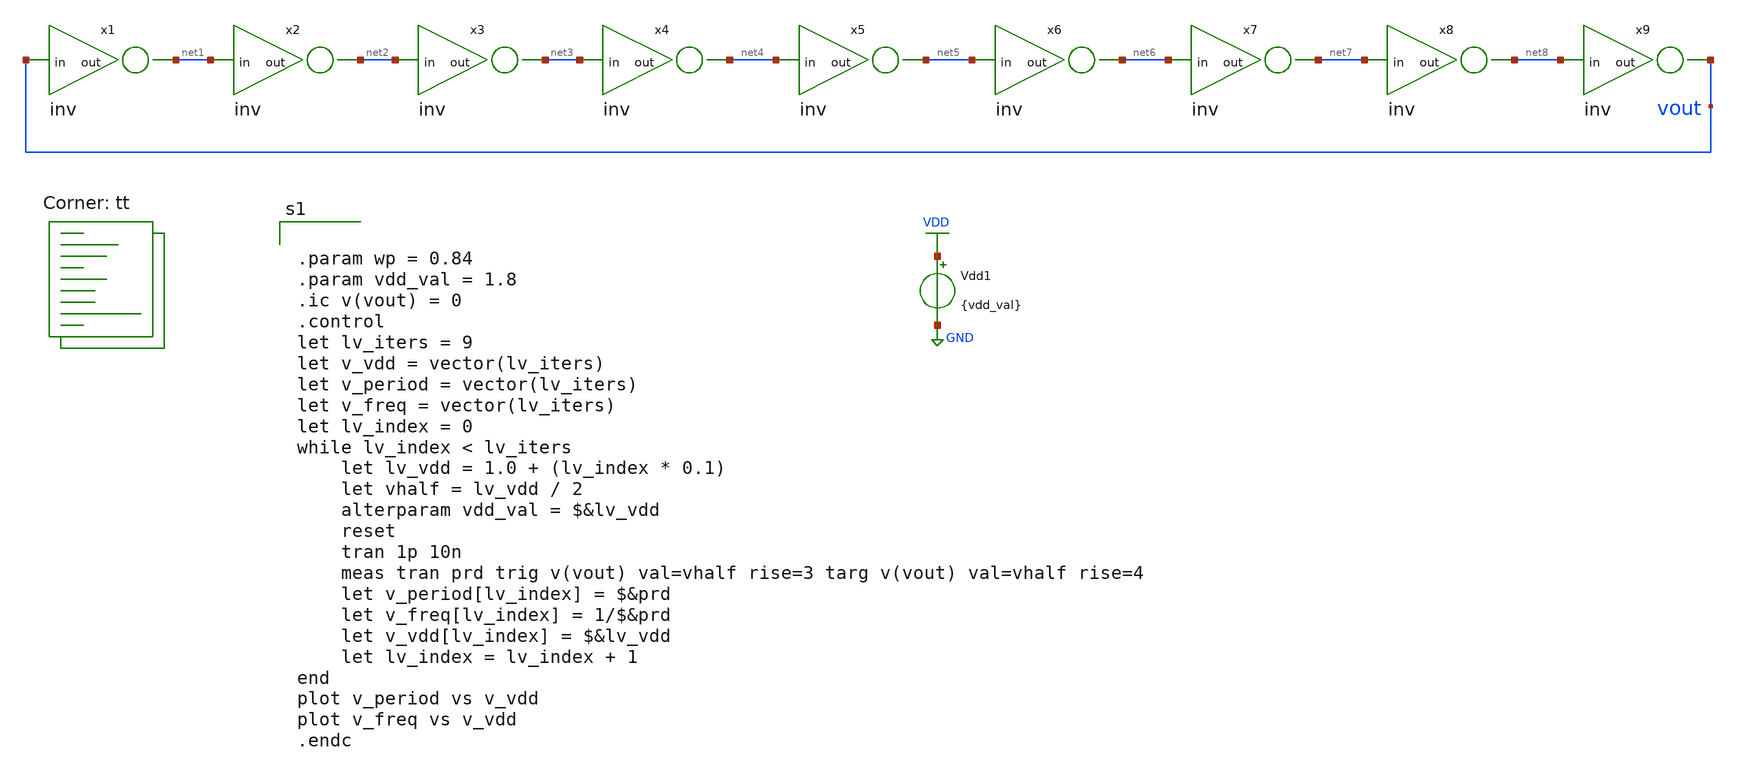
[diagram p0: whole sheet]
** sch_path: tut4/expt2/ro9.sch
**.subckt ro9
x1 net1 vout inv
x2 net2 net1 inv
x3 net3 net2 inv
x4 net4 net3 inv
x5 net5 net4 inv
x6 net6 net5 inv
x7 net7 net6 inv
Vdd1 VDD GND {vdd_val}
x8 net8 net7 inv
x9 vout net8 inv
**** begin user architecture code
.lib $::SKYWATER_MODELS/sky130.lib.spice tt


.param wp = 0.84
.param vdd_val = 1.8
.ic v(vout) = 0
.control
let lv_iters = 9
let v_vdd = vector(lv_iters)
let v_period = vector(lv_iters)
let v_freq = vector(lv_iters)
let lv_index = 0
while lv_index < lv_iters
	let lv_vdd = 1.0 + (lv_index * 0.1)
	let vhalf = lv_vdd / 2
	alterparam vdd_val = $&lv_vdd
	reset
	tran 1p 10n
	meas tran prd trig v(vout) val=vhalf rise=3 targ v(vout) val=vhalf rise=4
	let v_period[lv_index] = $&prd
	let v_freq[lv_index] = 1/$&prd
	let v_vdd[lv_index] = $&lv_vdd
	let lv_index = lv_index + 1
end
plot v_period vs v_vdd
plot v_freq vs v_vdd
.endc


**** end user architecture code
**.ends

* expanding   symbol:  /home/ee24s053/ee5311-2025/tut3/syms/inv.sym # of pins=2
** sym_path: tut3/syms/inv.sym
** sch_path: tut3/syms/inv.sch
.subckt inv out in
*.ipin in
*.opin out
XM1 out in VDD VDD sky130_fd_pr__pfet_01v8 L=0.15 W={wp} nf=1 ad='int((nf+1)/2) * W/nf * 0.29' as='int((nf+2)/2) * W/nf * 0.29'
+ pd='2*int((nf+1)/2) * (W/nf + 0.29)' ps='2*int((nf+2)/2) * (W/nf + 0.29)' nrd='0.29 / W' nrs='0.29 / W'
+ sa=0 sb=0 sd=0 mult=1 m=1
XM2 out in GND GND sky130_fd_pr__nfet_01v8 L=0.15 W=1 nf=1 ad='int((nf+1)/2) * W/nf * 0.29' as='int((nf+2)/2) * W/nf * 0.29'
+ pd='2*int((nf+1)/2) * (W/nf + 0.29)' ps='2*int((nf+2)/2) * (W/nf + 0.29)' nrd='0.29 / W' nrs='0.29 / W'
+ sa=0 sb=0 sd=0 mult=1 m=1
.ends

.GLOBAL VDD
.GLOBAL GND
.end
